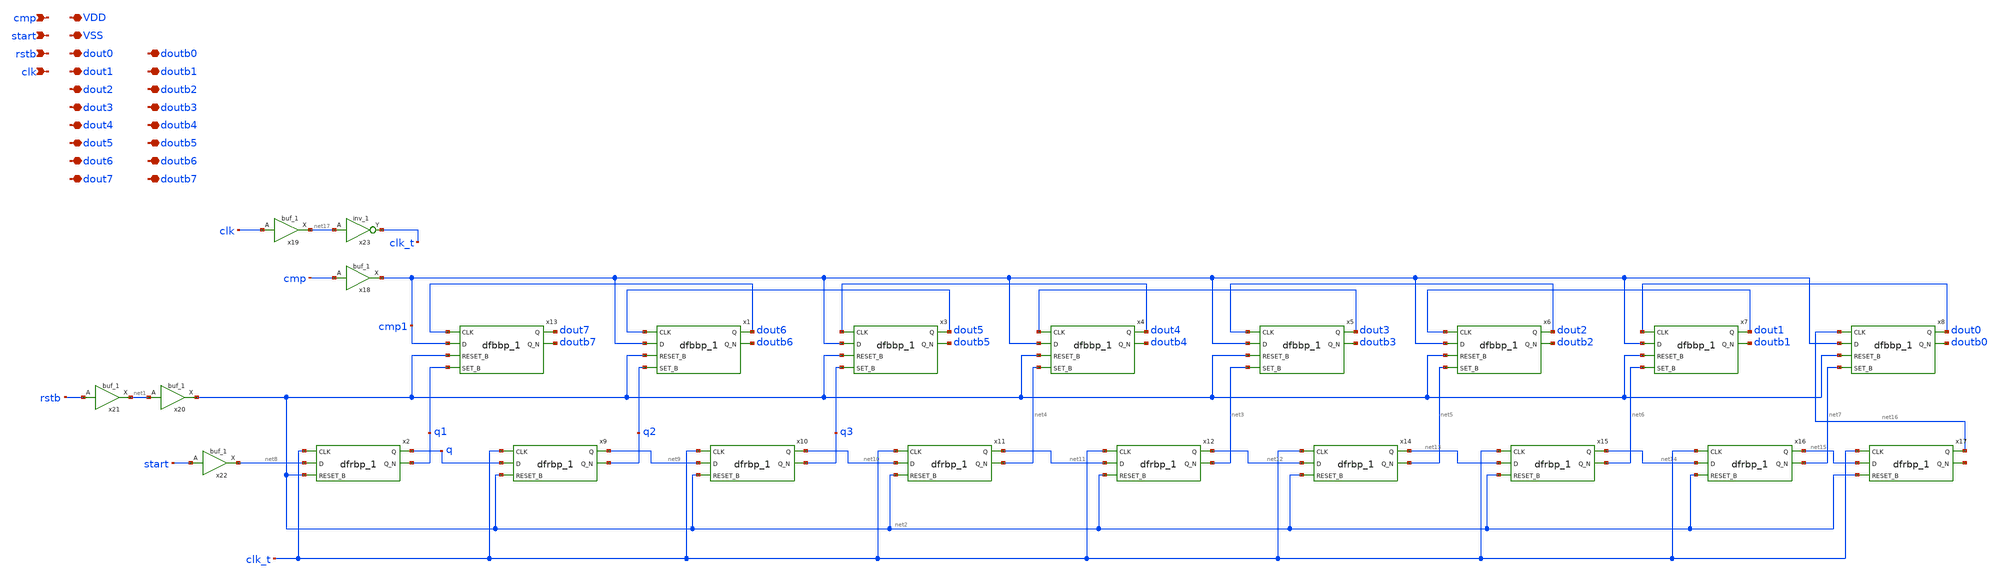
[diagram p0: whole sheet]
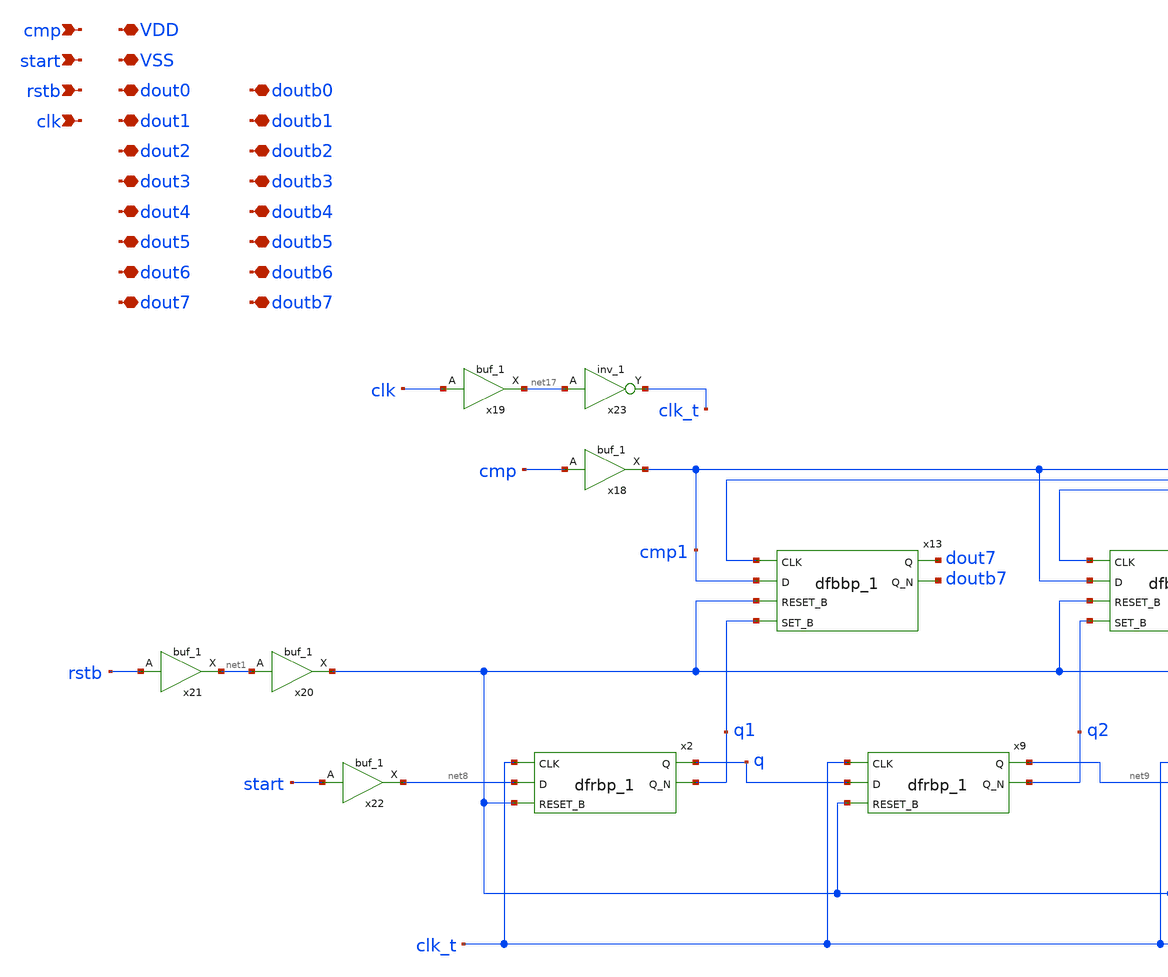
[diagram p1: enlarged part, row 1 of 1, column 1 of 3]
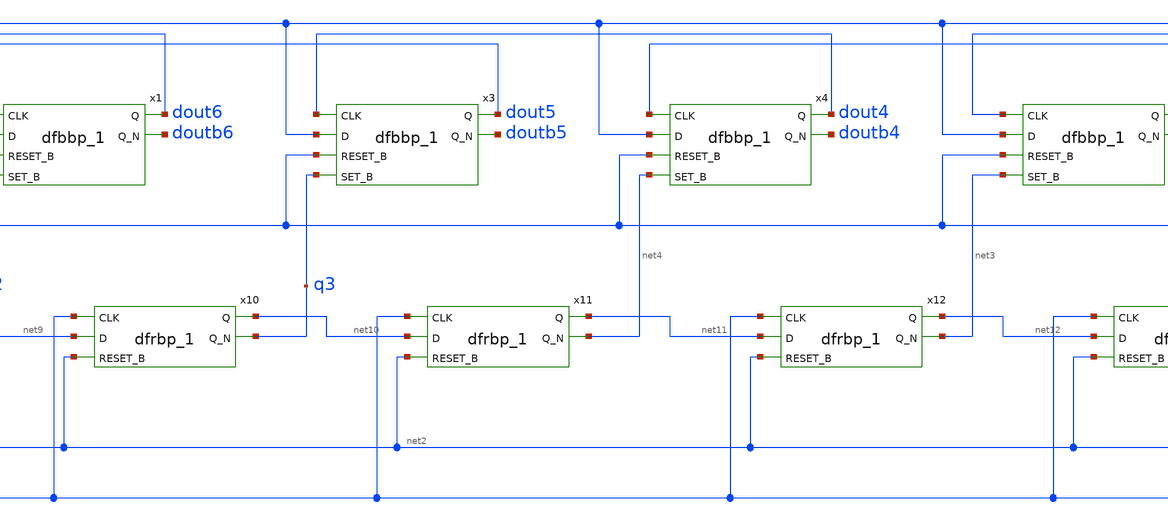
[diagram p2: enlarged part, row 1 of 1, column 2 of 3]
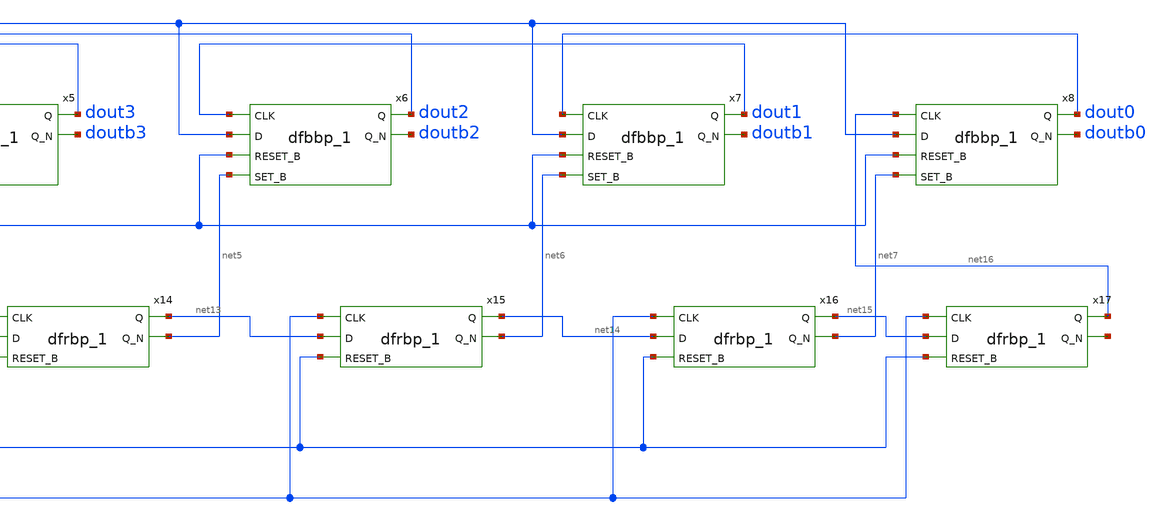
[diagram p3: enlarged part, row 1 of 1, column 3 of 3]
** sch_path: 8bitADC_SARLOGIC_pinout.sch
**.subckt 8bitADC_SARLOGIC_pinout cmp start rstb clk dout0 doutb0 VSS VDD dout1 dout2 dout3 dout4
*+ dout5 dout6 dout7 doutb1 doutb2 doutb3 doutb4 doutb5 doutb6 doutb7
*.ipin cmp
*.ipin start
*.ipin rstb
*.ipin clk
*.iopin dout0
*.iopin doutb0
*.iopin VSS
*.iopin VDD
*.iopin dout1
*.iopin dout2
*.iopin dout3
*.iopin dout4
*.iopin dout5
*.iopin dout6
*.iopin dout7
*.iopin doutb1
*.iopin doutb2
*.iopin doutb3
*.iopin doutb4
*.iopin doutb5
*.iopin doutb6
*.iopin doutb7
x18 cmp VSS VNB VPB VDD cmp1 sky130_fd_sc_hd__buf_1
x19 clk VSS VNB VPB VDD net17 sky130_fd_sc_hd__buf_1
x20 net1 VSS VNB VPB VDD net2 sky130_fd_sc_hd__buf_1
x21 rstb VSS VNB VPB VDD net1 sky130_fd_sc_hd__buf_1
x22 start VSS VNB VPB VDD net8 sky130_fd_sc_hd__buf_1
x2 clk_t net8 net2 VSS VNB VPB VDD q q1 sky130_fd_sc_hd__dfrbp_1
x9 clk_t q net2 VSS VNB VPB VDD net9 q2 sky130_fd_sc_hd__dfrbp_1
x10 clk_t net9 net2 VSS VNB VPB VDD net10 q3 sky130_fd_sc_hd__dfrbp_1
x11 clk_t net10 net2 VSS VNB VPB VDD net11 net4 sky130_fd_sc_hd__dfrbp_1
x12 clk_t net11 net2 VSS VNB VPB VDD net12 net3 sky130_fd_sc_hd__dfrbp_1
x14 clk_t net12 net2 VSS VNB VPB VDD net13 net5 sky130_fd_sc_hd__dfrbp_1
x15 clk_t net13 net2 VSS VNB VPB VDD net14 net6 sky130_fd_sc_hd__dfrbp_1
x16 clk_t net14 net2 VSS VNB VPB VDD net15 net7 sky130_fd_sc_hd__dfrbp_1
x17 clk_t net15 net2 VSS VNB VPB VDD net16 net18 sky130_fd_sc_hd__dfrbp_1
x23 net17 VSS VNB VPB VDD clk_t sky130_fd_sc_hd__inv_1
x13 dout6 cmp1 net2 q1 VSS VNB VPB VDD dout7 doutb7 sky130_fd_sc_hd__dfbbp_1
x1 dout5 cmp1 net2 q2 VSS VNB VPB VDD dout6 doutb6 sky130_fd_sc_hd__dfbbp_1
x3 dout4 cmp1 net2 q3 VSS VNB VPB VDD dout5 doutb5 sky130_fd_sc_hd__dfbbp_1
x4 dout3 cmp1 net2 net4 VSS VNB VPB VDD dout4 doutb4 sky130_fd_sc_hd__dfbbp_1
x5 dout2 cmp1 net2 net3 VSS VNB VPB VDD dout3 doutb3 sky130_fd_sc_hd__dfbbp_1
x6 dout1 cmp1 net2 net5 VSS VNB VPB VDD dout2 doutb2 sky130_fd_sc_hd__dfbbp_1
x7 dout0 cmp1 net2 net6 VSS VNB VPB VDD dout1 doutb1 sky130_fd_sc_hd__dfbbp_1
x8 net16 cmp1 net2 net7 VSS VNB VPB VDD dout0 doutb0 sky130_fd_sc_hd__dfbbp_1
**.ends
.end
